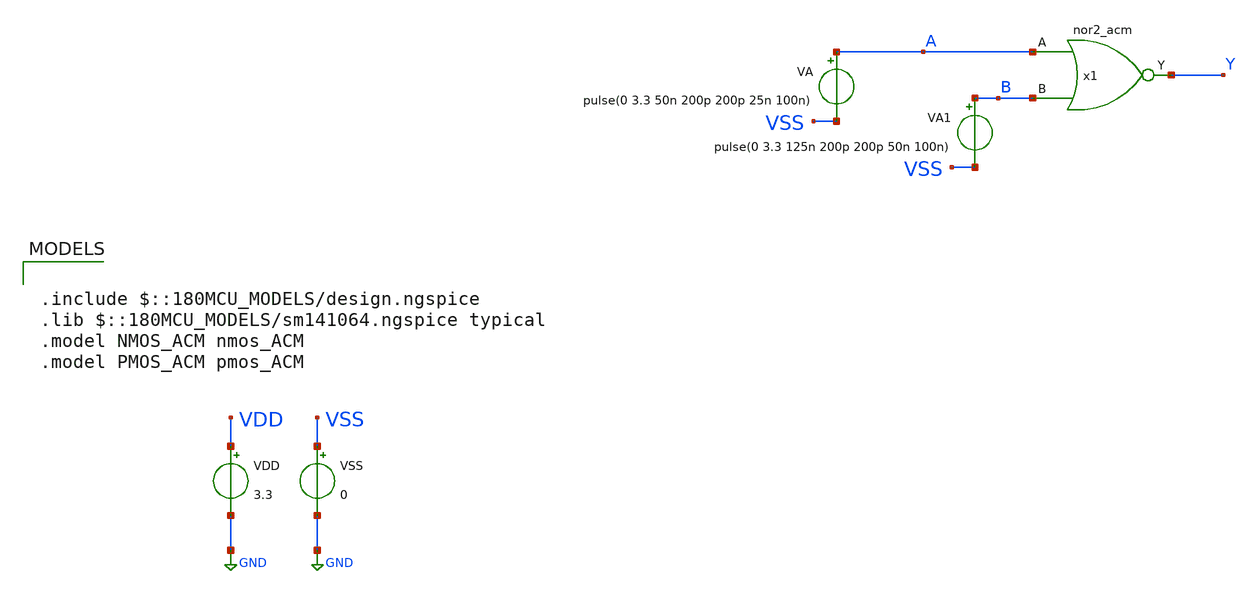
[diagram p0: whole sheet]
** sch_path: legacy/Examples/IHP-SG13/xschem/TB_nor2_acm.sch
**.subckt TB_nor2_acm
VA A VSS pulse(0 3.3 50n 200p 200p 25n 100n)
VDD VDD GND 3.3
VSS VSS GND 0
VA1 B VSS pulse(0 3.3 125n 200p 200p 50n 100n)
x1 A B Y VDD VSS nor2_acm
**** begin user architecture code

.include $::180MCU_MODELS/design.ngspice
.lib $::180MCU_MODELS/sm141064.ngspice typical
.model NMOS_ACM nmos_ACM
.model PMOS_ACM pmos_ACM



.option gmin=1e-15

.control
pre_osdi ./NMOS_ACM_2V0.osdi
pre_osdi ./PMOS_ACM_2V0.osdi
save all


tran 1n 500n
remzerovec
write TB_nor2_acm.raw
set appendwrite

.endc


**** end user architecture code
**.ends
.GLOBAL GND
.end
